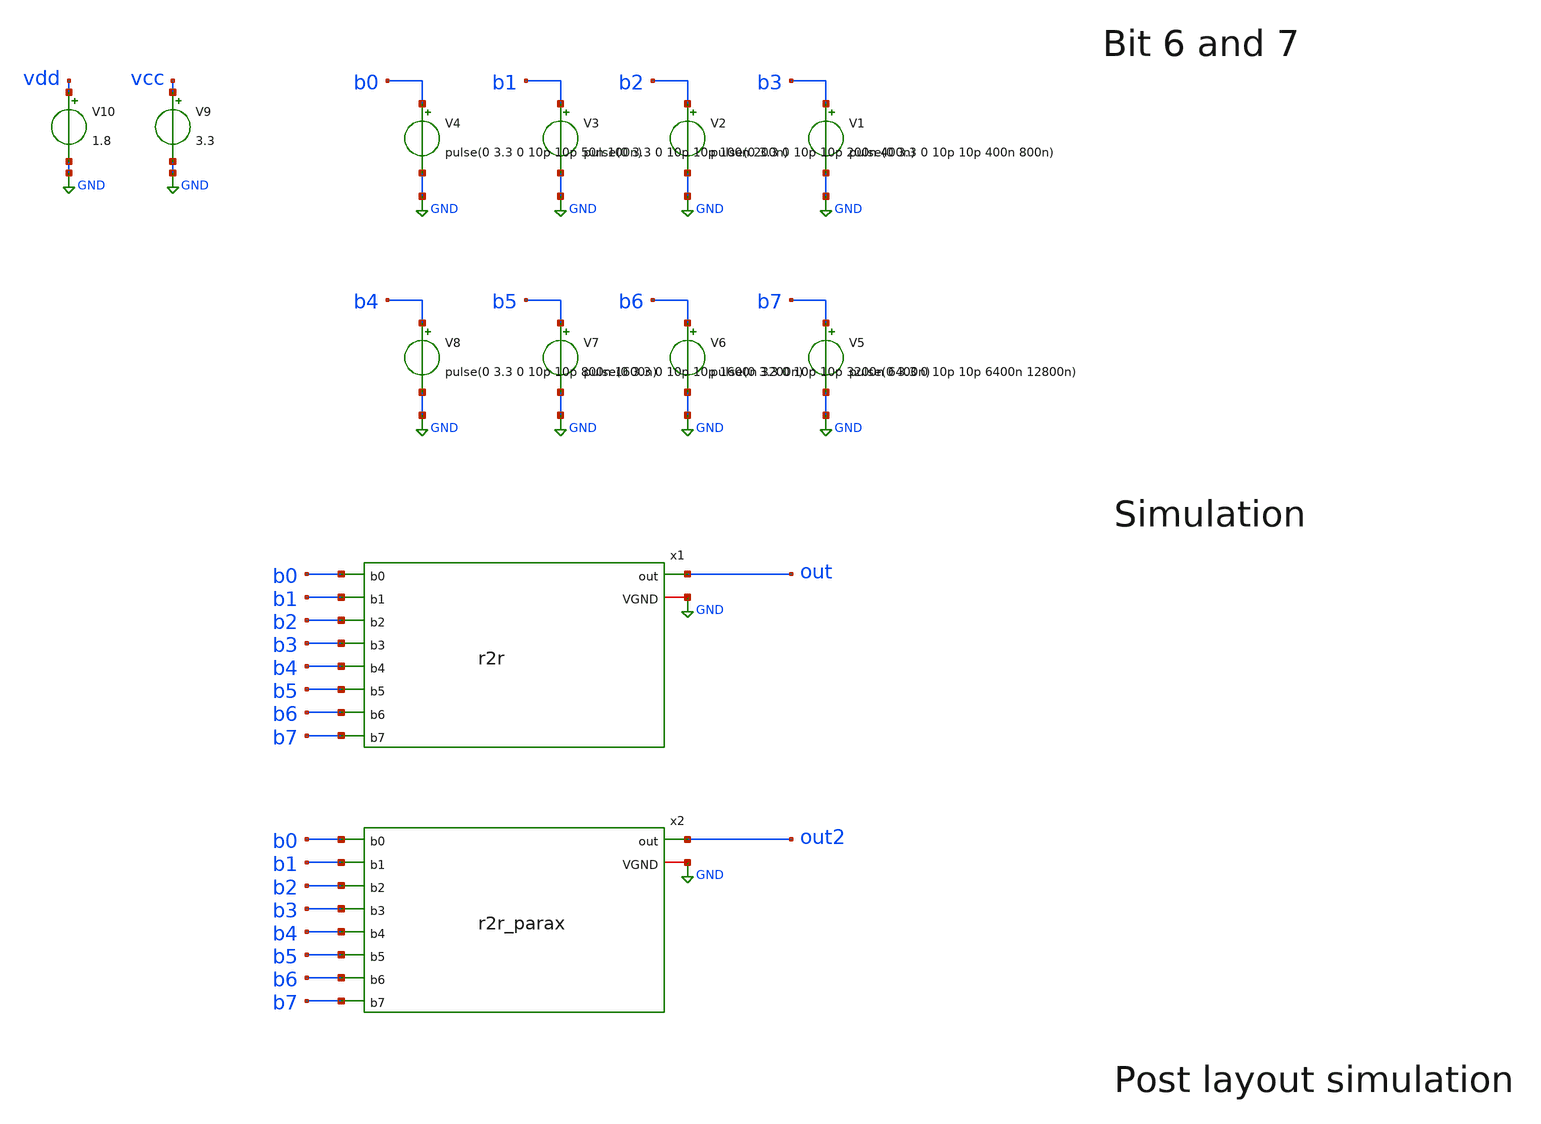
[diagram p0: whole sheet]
** sch_path: xschem/tb_r2r.sch
**.subckt tb_r2r
V1 b3 GND pulse(0 3.3 0 10p 10p 400n 800n)
V2 b2 GND pulse(0 3.3 0 10p 10p 200n 400n)
V3 b1 GND pulse(0 3.3 0 10p 10p 100n 200n)
V4 b0 GND pulse(0 3.3 0 10p 10p 50n 100n)
V5 b7 GND pulse(0 3.3 0 10p 10p 6400n 12800n)
V6 b6 GND pulse(0 3.3 0 10p 10p 3200n 6400n)
V7 b5 GND pulse(0 3.3 0 10p 10p 1600n 3200n)
V8 b4 GND pulse(0 3.3 0 10p 10p 800n 1600n)
V9 vcc GND 3.3
V10 vdd GND 1.8
x1 b7 b1 b0 b2 b3 b4 b5 b6 out GND r2r
x2 b7 b1 b0 b2 b3 b4 b5 b6 out2 GND r2r_parax
**** begin user architecture code

.include design.ngspice
.lib sm141064.ngspice typical
.lib sm141064.ngspice res_typical



* .options filetype=ascii
.control
*tran 1n 128n uic
tran 1n 14000n uic
write tb_dac.raw
.endc
.end


**** end user architecture code
**.ends

* expanding   symbol:  r2r.sym # of pins=10
** sym_path: xschem/r2r.sym
** sch_path: xschem/r2r.sch
.subckt r2r b7 b1 b0 b2 b3 b4 b5 b6 out VGND
*.iopin VGND
*.ipin b0
*.ipin b1
*.opin out
*.ipin b2
*.ipin b3
*.ipin b4
*.ipin b5
*.ipin b6
*.ipin b7
XR1 net1 b0 VGND ppolyf_u_1k r_width=2e-6 r_length=50e-6 m=1
XR2 net2 net1 VGND ppolyf_u_1k r_width=2e-6 r_length=50e-6 m=1
XR3 net3 net2 VGND ppolyf_u_1k r_width=2e-6 r_length=50e-6 m=1
XR4 VGND net3 VGND ppolyf_u_1k r_width=2e-6 r_length=50e-6 m=1
XR5 net4 net2 VGND ppolyf_u_1k r_width=2e-6 r_length=50e-6 m=1
XR6 net5 b1 VGND ppolyf_u_1k r_width=2e-6 r_length=50e-6 m=1
XR7 net4 net5 VGND ppolyf_u_1k r_width=2e-6 r_length=50e-6 m=1
XR8 net6 net4 VGND ppolyf_u_1k r_width=2e-6 r_length=50e-6 m=1
XR9 net7 b2 VGND ppolyf_u_1k r_width=2e-6 r_length=50e-6 m=1
XR10 net6 net7 VGND ppolyf_u_1k r_width=2e-6 r_length=50e-6 m=1
XR11 net8 net6 VGND ppolyf_u_1k r_width=2e-6 r_length=50e-6 m=1
XR12 net9 b3 VGND ppolyf_u_1k r_width=2e-6 r_length=50e-6 m=1
XR13 net8 net9 VGND ppolyf_u_1k r_width=2e-6 r_length=50e-6 m=1
XR14 net10 net8 VGND ppolyf_u_1k r_width=2e-6 r_length=50e-6 m=1
XR15 net11 b4 VGND ppolyf_u_1k r_width=2e-6 r_length=50e-6 m=1
XR16 net10 net11 VGND ppolyf_u_1k r_width=2e-6 r_length=50e-6 m=1
XR17 net12 net10 VGND ppolyf_u_1k r_width=2e-6 r_length=50e-6 m=1
XR18 net13 b5 VGND ppolyf_u_1k r_width=2e-6 r_length=50e-6 m=1
XR19 net12 net13 VGND ppolyf_u_1k r_width=2e-6 r_length=50e-6 m=1
XR20 net14 net12 VGND ppolyf_u_1k r_width=2e-6 r_length=50e-6 m=1
XR21 net15 b6 VGND ppolyf_u_1k r_width=2e-6 r_length=50e-6 m=1
XR22 net14 net15 VGND ppolyf_u_1k r_width=2e-6 r_length=50e-6 m=1
XR23 out net14 VGND ppolyf_u_1k r_width=2e-6 r_length=50e-6 m=1
XR24 net16 b7 VGND ppolyf_u_1k r_width=2e-6 r_length=50e-6 m=1
XR25 out net16 VGND ppolyf_u_1k r_width=2e-6 r_length=50e-6 m=1
XR26 VGND VGND VGND ppolyf_u_1k r_width=2e-6 r_length=50e-6 m=1
XR27 VGND VGND VGND ppolyf_u_1k r_width=2e-6 r_length=50e-6 m=1
.ends


* expanding   symbol:  r2r_parax.sym # of pins=10
** sym_path: xschem/r2r.sym
.include [file normalize ../mag/r2r.sim.spice]
.GLOBAL GND
.end
